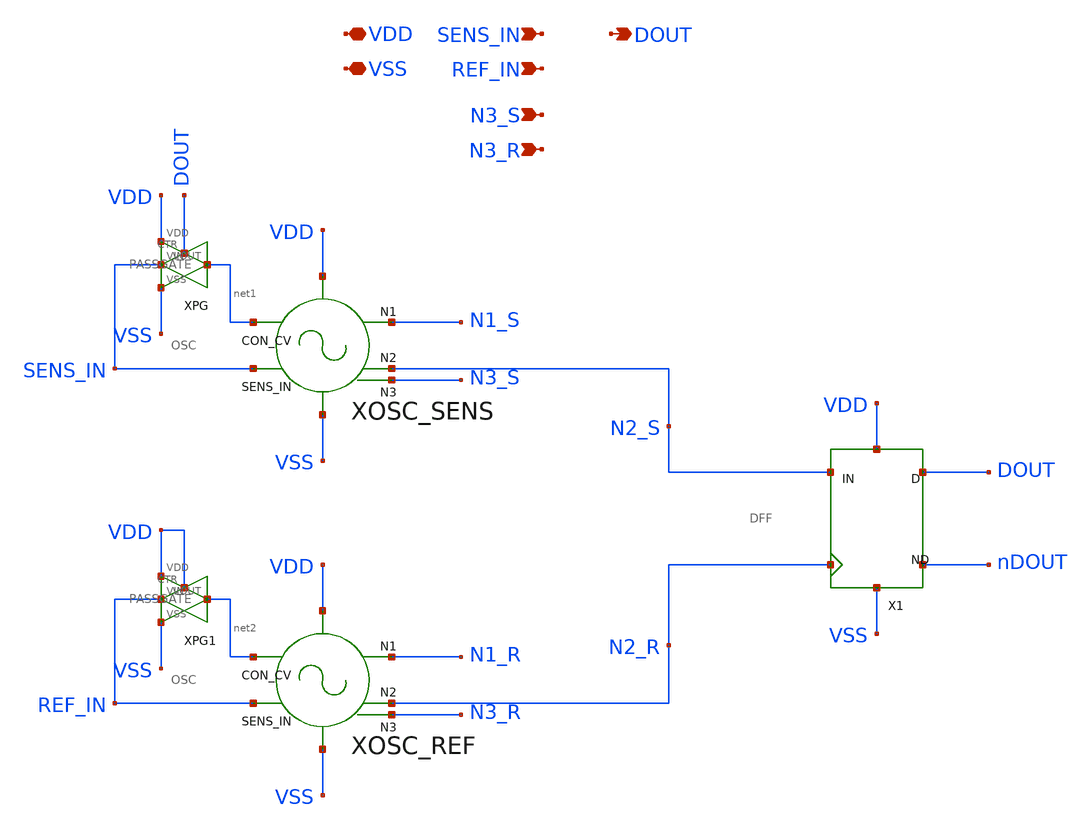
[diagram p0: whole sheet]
** sch_path: modules/INTERNAL_SDC/symbol/INTERNAL_SDC.sch
**.subckt INTERNAL_SDC VDD VSS SENS_IN REF_IN DOUT N3_S N3_R
*.iopin VDD
*.iopin VSS
*.ipin SENS_IN
*.ipin REF_IN
*.opin DOUT
*.ipin N3_S
*.ipin N3_R
XOSC_SENS SENS_IN N1_S N2_S VDD VSS net1 N3_S OSC
XOSC_REF REF_IN N1_R N2_R VDD VSS net2 N3_R OSC
XPG SENS_IN DOUT net1 VDD VSS PASSGATE
XPG1 REF_IN VDD net2 VDD VSS PASSGATE
X1 N2_S N2_R DOUT nDOUT VDD VSS DFF
**.ends
.end
